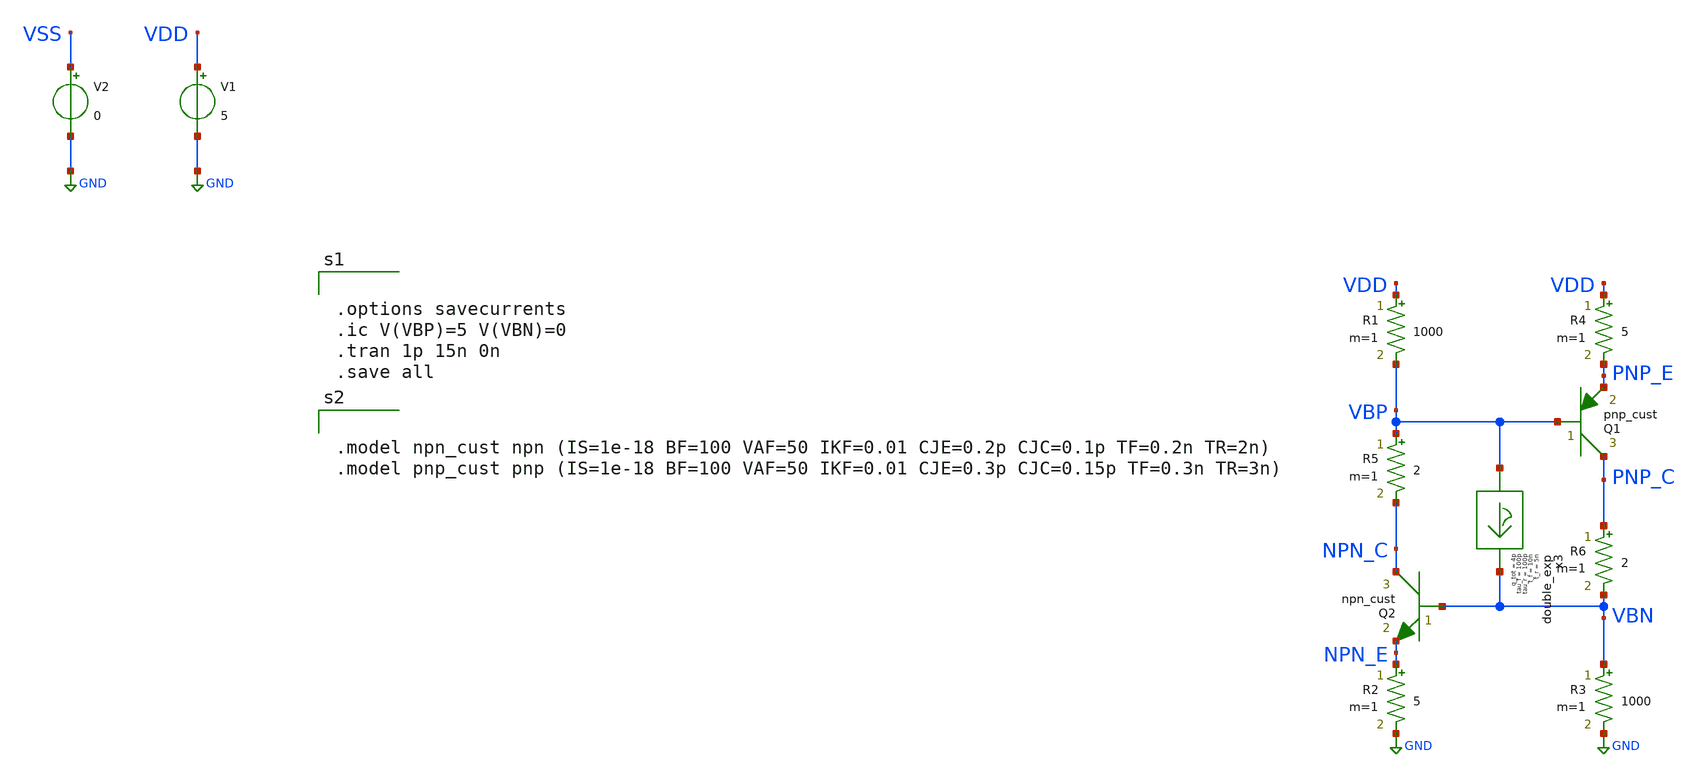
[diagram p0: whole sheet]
** sch_path: latchup/intermed_test.sch
**.subckt intermed_test
V1 VDD GND 5
V2 VSS GND 0
x3 VBP VBN double_exp t_r=5n tau_r=100p t_f=10n tau_f=100p q_tot=4p
Q1 PNP_C VBP PNP_E pnp_cust area=1 m=1
Q2 NPN_C VBN NPN_E npn_cust area=1 m=1
R3 VBN GND 1000 m=1
R4 VDD PNP_E 5 m=1
R1 VDD VBP 1000 m=1
R2 NPN_E GND 5 m=1
R5 VBP NPN_C 2 m=1
R6 PNP_C VBN 2 m=1
**** begin user architecture code


.options savecurrents
.ic V(VBP)=5 V(VBN)=0
.tran 1p 15n 0n
.save all




.include /usr/local/share/rad_modeling_blocks/rad_modeling_blocks.spice




.model npn_cust npn (IS=1e-18 BF=100 VAF=50 IKF=0.01 CJE=0.2p CJC=0.1p TF=0.2n TR=2n)
.model pnp_cust pnp (IS=1e-18 BF=100 VAF=50 IKF=0.01 CJE=0.3p CJC=0.15p TF=0.3n TR=3n)


**** end user architecture code
**.ends

* expanding   symbol:  double_exp.sym # of pins=2
** sym_path: xschem_rad_library/double_exp.sym
** sch_path: xschem_rad_library/double_exp.sch
.subckt double_exp in out  t_r=0 t_f=0 tau_r=0 tau_f=0 q_tot=0
*.opin OUT
*.ipin IN
I1 IN OUT EXP(0 {q_tot / (t_f-t_r+tau_f-tau_r)} {t_r} {tau_r} {t_f} {tau_f})
.ends

.GLOBAL GND
.end
